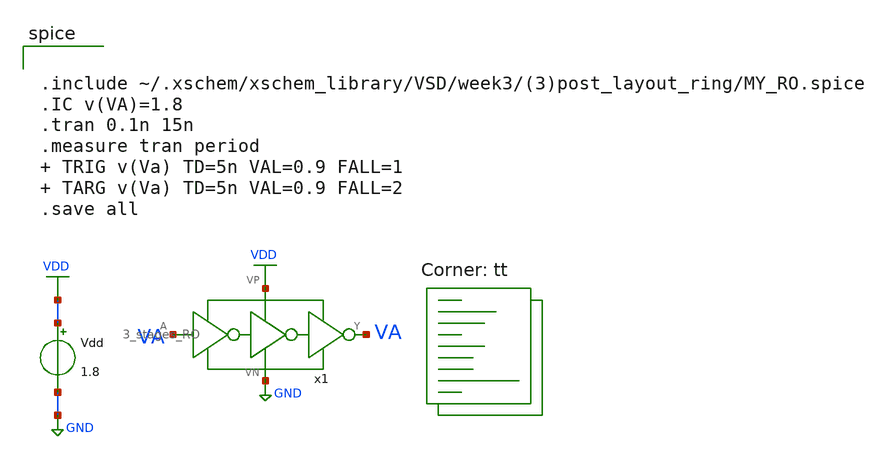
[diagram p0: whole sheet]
** sch_path: week 3/sim/4/RO_test.sch
**.subckt RO_test
Vdd VDD GND 1.8
x1 VA VDD VA GND 3_stages_RO
**** begin user architecture code


.include ~/.xschem/xschem_library/VSD/week3/(3)post_layout_ring/MY_RO.spice
.IC v(VA)=1.8
.tran 0.1n 15n
.measure tran period  TRIG v(Va) TD=5n VAL=0.9 FALL=1  TARG v(Va) TD=5n VAL=0.9 FALL=2
.save all

 .lib /usr/local/share/pdk/sky130A/libs.tech/ngspice/sky130.lib.spice tt
**** end user architecture code
**.ends
.GLOBAL VDD
.GLOBAL GND
.end
